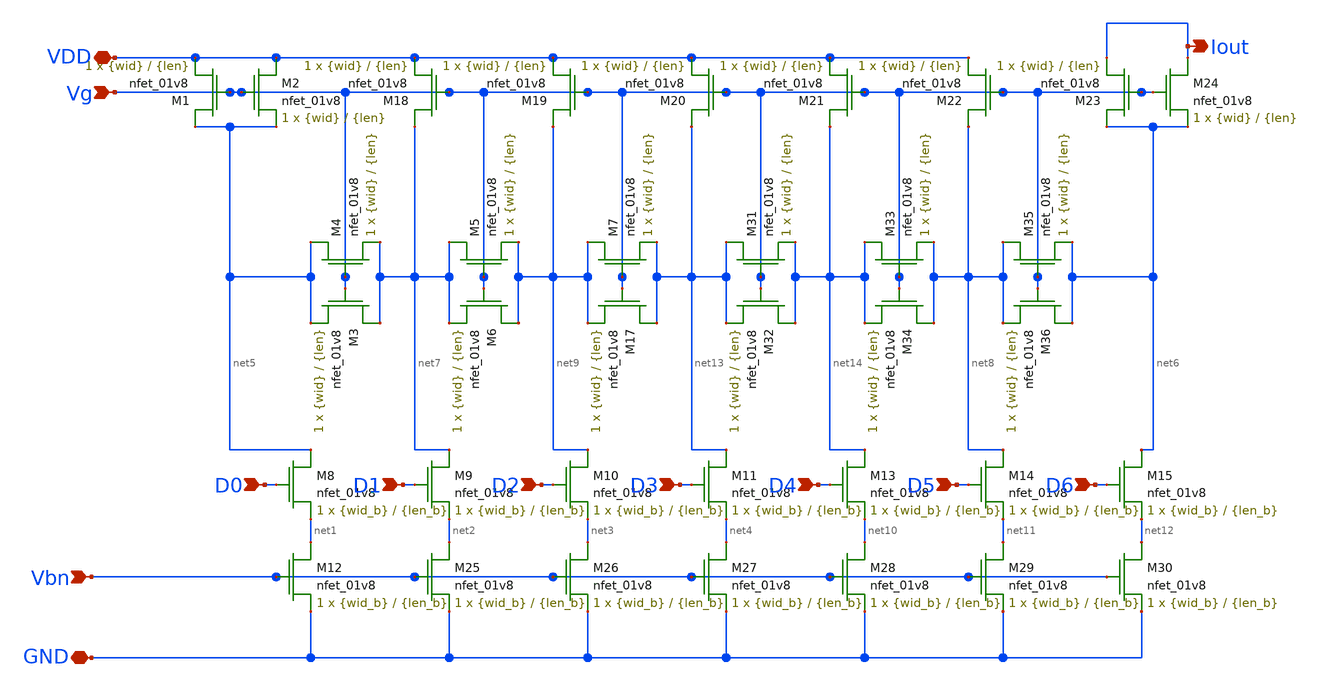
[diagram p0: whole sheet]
** sch_path: mp3/ladder.sch
**.subckt ladder Vbn VDD Iout GND D0 D1 D2 D3 D4 D5 D6 Vg
*.ipin Vbn
*.iopin VDD
*.opin Iout
*.iopin GND
*.ipin D0
*.ipin D1
*.ipin D2
*.ipin D3
*.ipin D4
*.ipin D5
*.ipin D6
*.ipin Vg
XM8 net5 D0 net1 GND sky130_fd_pr__nfet_01v8 L={len_b} W={wid_b} nf=1 ad='int((nf+1)/2) * W/nf * 0.29'
+ as='int((nf+2)/2) * W/nf * 0.29' pd='2*int((nf+1)/2) * (W/nf + 0.29)' ps='2*int((nf+2)/2) * (W/nf + 0.29)'
+ nrd='0.29 / W' nrs='0.29 / W' sa=0 sb=0 sd=0 mult=1 m=1
XM1 net5 Vg VDD GND sky130_fd_pr__nfet_01v8 L={len} W={wid} nf=1 ad='int((nf+1)/2) * W/nf * 0.29' as='int((nf+2)/2) * W/nf * 0.29'
+ pd='2*int((nf+1)/2) * (W/nf + 0.29)' ps='2*int((nf+2)/2) * (W/nf + 0.29)' nrd='0.29 / W' nrs='0.29 / W'
+ sa=0 sb=0 sd=0 mult=1 m=1
XM4 net5 Vg net7 GND sky130_fd_pr__nfet_01v8 L={len} W={wid} nf=1 ad='int((nf+1)/2) * W/nf * 0.29' as='int((nf+2)/2) * W/nf * 0.29'
+ pd='2*int((nf+1)/2) * (W/nf + 0.29)' ps='2*int((nf+2)/2) * (W/nf + 0.29)' nrd='0.29 / W' nrs='0.29 / W'
+ sa=0 sb=0 sd=0 mult=1 m=1
XM12 net1 Vbn GND GND sky130_fd_pr__nfet_01v8 L={len_b} W={wid_b} nf=1 ad='int((nf+1)/2) * W/nf * 0.29'
+ as='int((nf+2)/2) * W/nf * 0.29' pd='2*int((nf+1)/2) * (W/nf + 0.29)' ps='2*int((nf+2)/2) * (W/nf + 0.29)'
+ nrd='0.29 / W' nrs='0.29 / W' sa=0 sb=0 sd=0 mult=1 m=1
XM9 net7 D1 net2 GND sky130_fd_pr__nfet_01v8 L={len_b} W={wid_b} nf=1 ad='int((nf+1)/2) * W/nf * 0.29'
+ as='int((nf+2)/2) * W/nf * 0.29' pd='2*int((nf+1)/2) * (W/nf + 0.29)' ps='2*int((nf+2)/2) * (W/nf + 0.29)'
+ nrd='0.29 / W' nrs='0.29 / W' sa=0 sb=0 sd=0 mult=1 m=1
XM10 net9 D2 net3 GND sky130_fd_pr__nfet_01v8 L={len_b} W={wid_b} nf=1 ad='int((nf+1)/2) * W/nf * 0.29'
+ as='int((nf+2)/2) * W/nf * 0.29' pd='2*int((nf+1)/2) * (W/nf + 0.29)' ps='2*int((nf+2)/2) * (W/nf + 0.29)'
+ nrd='0.29 / W' nrs='0.29 / W' sa=0 sb=0 sd=0 mult=1 m=1
XM11 net13 D3 net4 GND sky130_fd_pr__nfet_01v8 L={len_b} W={wid_b} nf=1 ad='int((nf+1)/2) * W/nf * 0.29'
+ as='int((nf+2)/2) * W/nf * 0.29' pd='2*int((nf+1)/2) * (W/nf + 0.29)' ps='2*int((nf+2)/2) * (W/nf + 0.29)'
+ nrd='0.29 / W' nrs='0.29 / W' sa=0 sb=0 sd=0 mult=1 m=1
XM13 net14 D4 net10 GND sky130_fd_pr__nfet_01v8 L={len_b} W={wid_b} nf=1 ad='int((nf+1)/2) * W/nf * 0.29'
+ as='int((nf+2)/2) * W/nf * 0.29' pd='2*int((nf+1)/2) * (W/nf + 0.29)' ps='2*int((nf+2)/2) * (W/nf + 0.29)'
+ nrd='0.29 / W' nrs='0.29 / W' sa=0 sb=0 sd=0 mult=1 m=1
XM14 net8 D5 net11 GND sky130_fd_pr__nfet_01v8 L={len_b} W={wid_b} nf=1 ad='int((nf+1)/2) * W/nf * 0.29'
+ as='int((nf+2)/2) * W/nf * 0.29' pd='2*int((nf+1)/2) * (W/nf + 0.29)' ps='2*int((nf+2)/2) * (W/nf + 0.29)'
+ nrd='0.29 / W' nrs='0.29 / W' sa=0 sb=0 sd=0 mult=1 m=1
XM15 net6 D6 net12 GND sky130_fd_pr__nfet_01v8 L={len_b} W={wid_b} nf=1 ad='int((nf+1)/2) * W/nf * 0.29'
+ as='int((nf+2)/2) * W/nf * 0.29' pd='2*int((nf+1)/2) * (W/nf + 0.29)' ps='2*int((nf+2)/2) * (W/nf + 0.29)'
+ nrd='0.29 / W' nrs='0.29 / W' sa=0 sb=0 sd=0 mult=1 m=1
XM25 net2 Vbn GND GND sky130_fd_pr__nfet_01v8 L={len_b} W={wid_b} nf=1 ad='int((nf+1)/2) * W/nf * 0.29'
+ as='int((nf+2)/2) * W/nf * 0.29' pd='2*int((nf+1)/2) * (W/nf + 0.29)' ps='2*int((nf+2)/2) * (W/nf + 0.29)'
+ nrd='0.29 / W' nrs='0.29 / W' sa=0 sb=0 sd=0 mult=1 m=1
XM26 net3 Vbn GND GND sky130_fd_pr__nfet_01v8 L={len_b} W={wid_b} nf=1 ad='int((nf+1)/2) * W/nf * 0.29'
+ as='int((nf+2)/2) * W/nf * 0.29' pd='2*int((nf+1)/2) * (W/nf + 0.29)' ps='2*int((nf+2)/2) * (W/nf + 0.29)'
+ nrd='0.29 / W' nrs='0.29 / W' sa=0 sb=0 sd=0 mult=1 m=1
XM27 net4 Vbn GND GND sky130_fd_pr__nfet_01v8 L={len_b} W={wid_b} nf=1 ad='int((nf+1)/2) * W/nf * 0.29'
+ as='int((nf+2)/2) * W/nf * 0.29' pd='2*int((nf+1)/2) * (W/nf + 0.29)' ps='2*int((nf+2)/2) * (W/nf + 0.29)'
+ nrd='0.29 / W' nrs='0.29 / W' sa=0 sb=0 sd=0 mult=1 m=1
XM28 net10 Vbn GND GND sky130_fd_pr__nfet_01v8 L={len_b} W={wid_b} nf=1 ad='int((nf+1)/2) * W/nf * 0.29'
+ as='int((nf+2)/2) * W/nf * 0.29' pd='2*int((nf+1)/2) * (W/nf + 0.29)' ps='2*int((nf+2)/2) * (W/nf + 0.29)'
+ nrd='0.29 / W' nrs='0.29 / W' sa=0 sb=0 sd=0 mult=1 m=1
XM29 net11 Vbn GND GND sky130_fd_pr__nfet_01v8 L={len_b} W={wid_b} nf=1 ad='int((nf+1)/2) * W/nf * 0.29'
+ as='int((nf+2)/2) * W/nf * 0.29' pd='2*int((nf+1)/2) * (W/nf + 0.29)' ps='2*int((nf+2)/2) * (W/nf + 0.29)'
+ nrd='0.29 / W' nrs='0.29 / W' sa=0 sb=0 sd=0 mult=1 m=1
XM30 net12 Vbn GND GND sky130_fd_pr__nfet_01v8 L={len_b} W={wid_b} nf=1 ad='int((nf+1)/2) * W/nf * 0.29'
+ as='int((nf+2)/2) * W/nf * 0.29' pd='2*int((nf+1)/2) * (W/nf + 0.29)' ps='2*int((nf+2)/2) * (W/nf + 0.29)'
+ nrd='0.29 / W' nrs='0.29 / W' sa=0 sb=0 sd=0 mult=1 m=1
XM2 VDD Vg net5 GND sky130_fd_pr__nfet_01v8 L={len} W={wid} nf=1 ad='int((nf+1)/2) * W/nf * 0.29' as='int((nf+2)/2) * W/nf * 0.29'
+ pd='2*int((nf+1)/2) * (W/nf + 0.29)' ps='2*int((nf+2)/2) * (W/nf + 0.29)' nrd='0.29 / W' nrs='0.29 / W'
+ sa=0 sb=0 sd=0 mult=1 m=1
XM18 net7 Vg VDD GND sky130_fd_pr__nfet_01v8 L={len} W={wid} nf=1 ad='int((nf+1)/2) * W/nf * 0.29' as='int((nf+2)/2) * W/nf * 0.29'
+ pd='2*int((nf+1)/2) * (W/nf + 0.29)' ps='2*int((nf+2)/2) * (W/nf + 0.29)' nrd='0.29 / W' nrs='0.29 / W'
+ sa=0 sb=0 sd=0 mult=1 m=1
XM19 net9 Vg VDD GND sky130_fd_pr__nfet_01v8 L={len} W={wid} nf=1 ad='int((nf+1)/2) * W/nf * 0.29' as='int((nf+2)/2) * W/nf * 0.29'
+ pd='2*int((nf+1)/2) * (W/nf + 0.29)' ps='2*int((nf+2)/2) * (W/nf + 0.29)' nrd='0.29 / W' nrs='0.29 / W'
+ sa=0 sb=0 sd=0 mult=1 m=1
XM20 net13 Vg VDD GND sky130_fd_pr__nfet_01v8 L={len} W={wid} nf=1 ad='int((nf+1)/2) * W/nf * 0.29' as='int((nf+2)/2) * W/nf * 0.29'
+ pd='2*int((nf+1)/2) * (W/nf + 0.29)' ps='2*int((nf+2)/2) * (W/nf + 0.29)' nrd='0.29 / W' nrs='0.29 / W'
+ sa=0 sb=0 sd=0 mult=1 m=1
XM21 net14 Vg VDD GND sky130_fd_pr__nfet_01v8 L={len} W={wid} nf=1 ad='int((nf+1)/2) * W/nf * 0.29' as='int((nf+2)/2) * W/nf * 0.29'
+ pd='2*int((nf+1)/2) * (W/nf + 0.29)' ps='2*int((nf+2)/2) * (W/nf + 0.29)' nrd='0.29 / W' nrs='0.29 / W'
+ sa=0 sb=0 sd=0 mult=1 m=1
XM22 net8 Vg VDD GND sky130_fd_pr__nfet_01v8 L={len} W={wid} nf=1 ad='int((nf+1)/2) * W/nf * 0.29' as='int((nf+2)/2) * W/nf * 0.29'
+ pd='2*int((nf+1)/2) * (W/nf + 0.29)' ps='2*int((nf+2)/2) * (W/nf + 0.29)' nrd='0.29 / W' nrs='0.29 / W'
+ sa=0 sb=0 sd=0 mult=1 m=1
XM23 net6 Vg Iout GND sky130_fd_pr__nfet_01v8 L={len} W={wid} nf=1 ad='int((nf+1)/2) * W/nf * 0.29' as='int((nf+2)/2) * W/nf * 0.29'
+ pd='2*int((nf+1)/2) * (W/nf + 0.29)' ps='2*int((nf+2)/2) * (W/nf + 0.29)' nrd='0.29 / W' nrs='0.29 / W'
+ sa=0 sb=0 sd=0 mult=1 m=1
XM24 Iout Vg net6 GND sky130_fd_pr__nfet_01v8 L={len} W={wid} nf=1 ad='int((nf+1)/2) * W/nf * 0.29' as='int((nf+2)/2) * W/nf * 0.29'
+ pd='2*int((nf+1)/2) * (W/nf + 0.29)' ps='2*int((nf+2)/2) * (W/nf + 0.29)' nrd='0.29 / W' nrs='0.29 / W'
+ sa=0 sb=0 sd=0 mult=1 m=1
XM3 net7 Vg net5 GND sky130_fd_pr__nfet_01v8 L={len} W={wid} nf=1 ad='int((nf+1)/2) * W/nf * 0.29' as='int((nf+2)/2) * W/nf * 0.29'
+ pd='2*int((nf+1)/2) * (W/nf + 0.29)' ps='2*int((nf+2)/2) * (W/nf + 0.29)' nrd='0.29 / W' nrs='0.29 / W'
+ sa=0 sb=0 sd=0 mult=1 m=1
XM5 net7 Vg net9 GND sky130_fd_pr__nfet_01v8 L={len} W={wid} nf=1 ad='int((nf+1)/2) * W/nf * 0.29' as='int((nf+2)/2) * W/nf * 0.29'
+ pd='2*int((nf+1)/2) * (W/nf + 0.29)' ps='2*int((nf+2)/2) * (W/nf + 0.29)' nrd='0.29 / W' nrs='0.29 / W'
+ sa=0 sb=0 sd=0 mult=1 m=1
XM6 net9 Vg net7 GND sky130_fd_pr__nfet_01v8 L={len} W={wid} nf=1 ad='int((nf+1)/2) * W/nf * 0.29' as='int((nf+2)/2) * W/nf * 0.29'
+ pd='2*int((nf+1)/2) * (W/nf + 0.29)' ps='2*int((nf+2)/2) * (W/nf + 0.29)' nrd='0.29 / W' nrs='0.29 / W'
+ sa=0 sb=0 sd=0 mult=1 m=1
XM7 net9 Vg net13 GND sky130_fd_pr__nfet_01v8 L={len} W={wid} nf=1 ad='int((nf+1)/2) * W/nf * 0.29' as='int((nf+2)/2) * W/nf * 0.29'
+ pd='2*int((nf+1)/2) * (W/nf + 0.29)' ps='2*int((nf+2)/2) * (W/nf + 0.29)' nrd='0.29 / W' nrs='0.29 / W'
+ sa=0 sb=0 sd=0 mult=1 m=1
XM17 net13 Vg net9 GND sky130_fd_pr__nfet_01v8 L={len} W={wid} nf=1 ad='int((nf+1)/2) * W/nf * 0.29'
+ as='int((nf+2)/2) * W/nf * 0.29' pd='2*int((nf+1)/2) * (W/nf + 0.29)' ps='2*int((nf+2)/2) * (W/nf + 0.29)'
+ nrd='0.29 / W' nrs='0.29 / W' sa=0 sb=0 sd=0 mult=1 m=1
XM31 net13 Vg net14 GND sky130_fd_pr__nfet_01v8 L={len} W={wid} nf=1 ad='int((nf+1)/2) * W/nf * 0.29'
+ as='int((nf+2)/2) * W/nf * 0.29' pd='2*int((nf+1)/2) * (W/nf + 0.29)' ps='2*int((nf+2)/2) * (W/nf + 0.29)'
+ nrd='0.29 / W' nrs='0.29 / W' sa=0 sb=0 sd=0 mult=1 m=1
XM32 net14 Vg net13 GND sky130_fd_pr__nfet_01v8 L={len} W={wid} nf=1 ad='int((nf+1)/2) * W/nf * 0.29'
+ as='int((nf+2)/2) * W/nf * 0.29' pd='2*int((nf+1)/2) * (W/nf + 0.29)' ps='2*int((nf+2)/2) * (W/nf + 0.29)'
+ nrd='0.29 / W' nrs='0.29 / W' sa=0 sb=0 sd=0 mult=1 m=1
XM33 net14 Vg net8 GND sky130_fd_pr__nfet_01v8 L={len} W={wid} nf=1 ad='int((nf+1)/2) * W/nf * 0.29'
+ as='int((nf+2)/2) * W/nf * 0.29' pd='2*int((nf+1)/2) * (W/nf + 0.29)' ps='2*int((nf+2)/2) * (W/nf + 0.29)'
+ nrd='0.29 / W' nrs='0.29 / W' sa=0 sb=0 sd=0 mult=1 m=1
XM34 net8 Vg net14 GND sky130_fd_pr__nfet_01v8 L={len} W={wid} nf=1 ad='int((nf+1)/2) * W/nf * 0.29'
+ as='int((nf+2)/2) * W/nf * 0.29' pd='2*int((nf+1)/2) * (W/nf + 0.29)' ps='2*int((nf+2)/2) * (W/nf + 0.29)'
+ nrd='0.29 / W' nrs='0.29 / W' sa=0 sb=0 sd=0 mult=1 m=1
XM35 net8 Vg net6 GND sky130_fd_pr__nfet_01v8 L={len} W={wid} nf=1 ad='int((nf+1)/2) * W/nf * 0.29' as='int((nf+2)/2) * W/nf * 0.29'
+ pd='2*int((nf+1)/2) * (W/nf + 0.29)' ps='2*int((nf+2)/2) * (W/nf + 0.29)' nrd='0.29 / W' nrs='0.29 / W'
+ sa=0 sb=0 sd=0 mult=1 m=1
XM36 net6 Vg net8 GND sky130_fd_pr__nfet_01v8 L={len} W={wid} nf=1 ad='int((nf+1)/2) * W/nf * 0.29' as='int((nf+2)/2) * W/nf * 0.29'
+ pd='2*int((nf+1)/2) * (W/nf + 0.29)' ps='2*int((nf+2)/2) * (W/nf + 0.29)' nrd='0.29 / W' nrs='0.29 / W'
+ sa=0 sb=0 sd=0 mult=1 m=1
**.ends
.end
